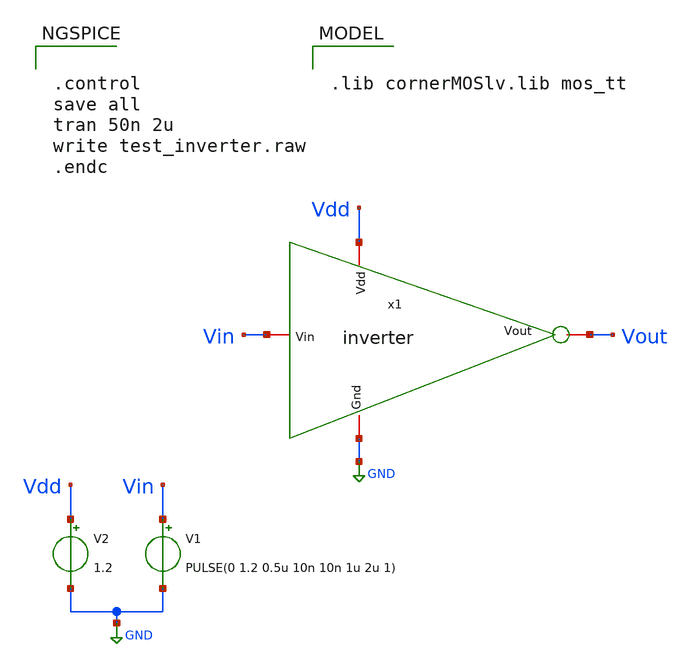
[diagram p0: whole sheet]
** sch_path: tests/data/_invcheck/inverter_tb_from_core_export.sch
**.subckt inverter_tb_from_core_export
V1 Vin GND PULSE(0 1.2 0.5u 10n 10n 1u 2u 1)
V2 Vdd GND 1.2
**** begin user architecture code


.control
save all
tran 50n 2u
write test_inverter.raw
.endc



.lib cornerMOSlv.lib mos_tt

**** end user architecture code
**.ends
.GLOBAL GND
.end
